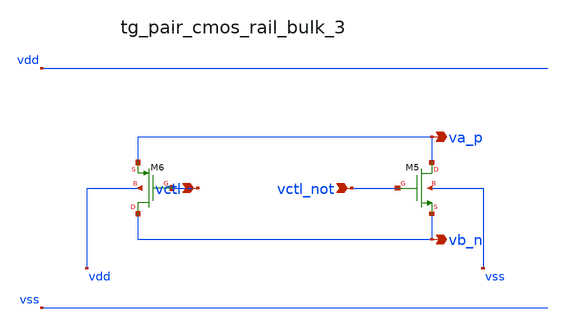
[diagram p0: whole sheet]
** sch_path: analog-db/raw/sw_002_chopper_diff/hier/blocks/tg_pair_cmos_rail_bulk_3.sch
**.subckt tg_pair_cmos_rail_bulk_3 vctl vctl_not va_p vb_n
*.ipin vctl
*.ipin vctl_not
*.opin va_p
*.opin vb_n
XM5 va_p vctl_not vb_n vss sg13_lv_nmos w=x_dut_xm5_w l=x_dut_xm5_l ng=1 m=x_dut_xm5_m
XM6 vb_n vctl va_p vdd sg13_lv_pmos w=x_dut_xm6_w l=x_dut_xm6_l ng=1 m=x_dut_xm6_m
**.ends
.end
